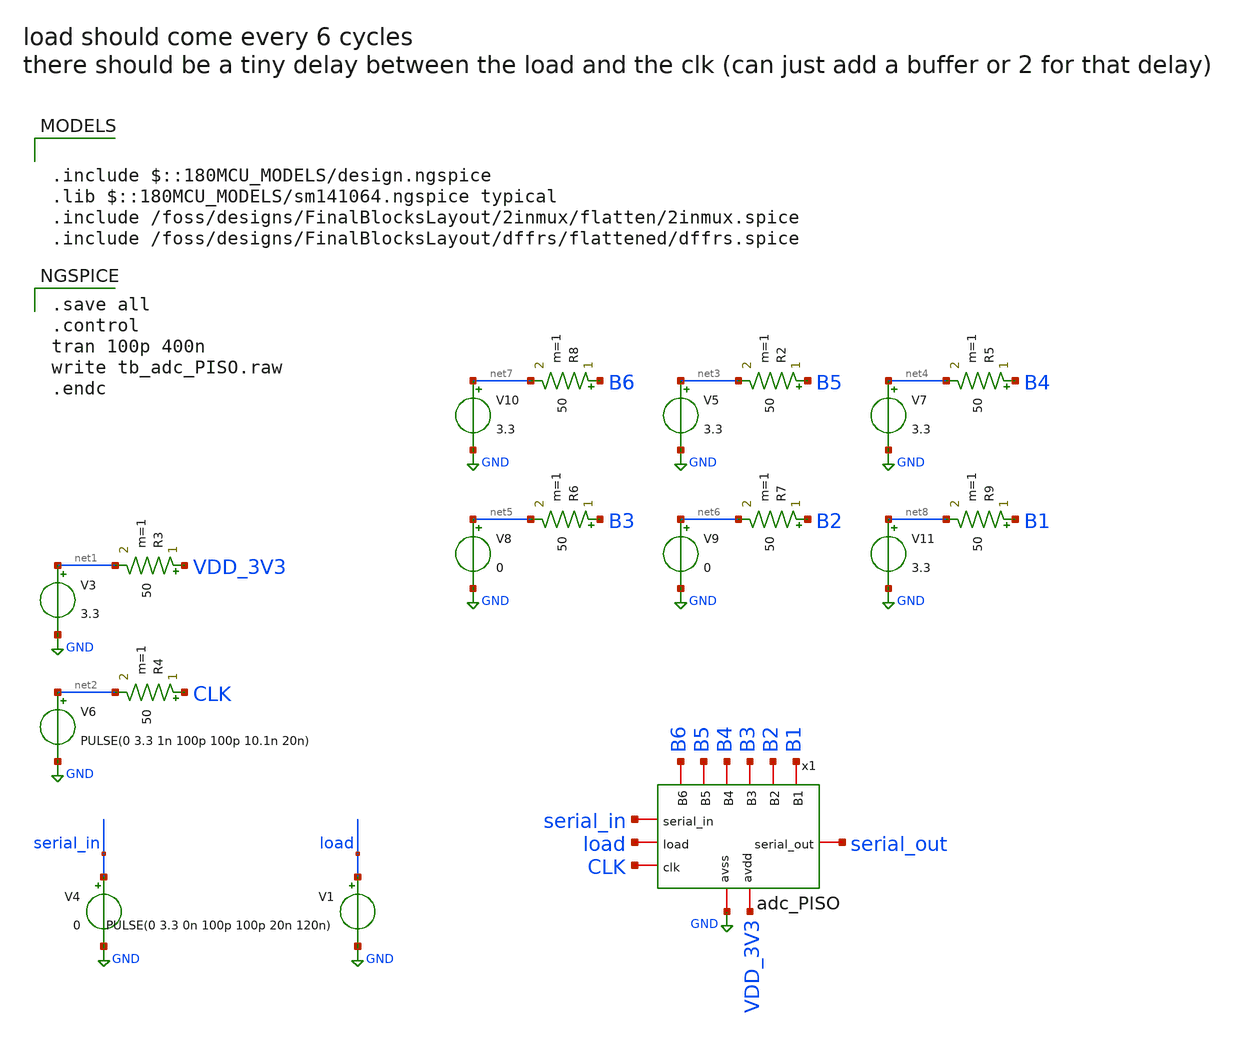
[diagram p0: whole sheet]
** sch_path: designs/FinalBlocksLayout/piso/tb_adc_PISO.sch
**.subckt tb_adc_PISO
V3 net1 GND 3.3
V6 net2 GND PULSE(0 3.3 1n 100p 100p 10.1n 20n)
R3 VDD_3V3 net1 50 m=1
R4 CLK net2 50 m=1
V4 serial_in GND 0
V1 load GND PULSE(0 3.3 0n 100p 100p 20n 120n)
V5 net3 GND 3.3
R2 B5 net3 50 m=1
V7 net4 GND 3.3
R5 B4 net4 50 m=1
V8 net5 GND 0
R6 B3 net5 50 m=1
V9 net6 GND 0
R7 B2 net6 50 m=1
V10 net7 GND 3.3
R8 B6 net7 50 m=1
V11 net8 GND 3.3
R9 B1 net8 50 m=1
x1 load serial_in B6 B5 B4 serial_out VDD_3V3 B3 GND B2 B1 CLK adc_PISO
**** begin user architecture code

.include $::180MCU_MODELS/design.ngspice
.lib $::180MCU_MODELS/sm141064.ngspice typical
.include /foss/designs/FinalBlocksLayout/2inmux/flatten/2inmux.spice
.include /foss/designs/FinalBlocksLayout/dffrs/flattened/dffrs.spice


.save all
.control
tran 100p 400n
write tb_adc_PISO.raw
.endc

**** end user architecture code
**.ends
.GLOBAL GND
.end
